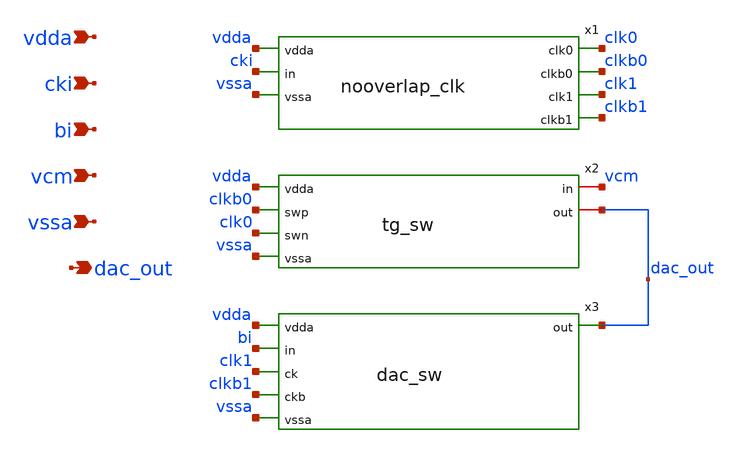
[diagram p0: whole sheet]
** sch_path: xschem/cdac_sw.sch
**.subckt cdac_sw vdda cki bi vcm vssa dac_out
*.ipin vdda
*.ipin cki
*.ipin bi
*.ipin vcm
*.ipin vssa
*.opin dac_out
x1 vdda cki vssa clk0 clkb0 clk1 clkb1 nooverlap_clk
x2 vdda clkb0 clk0 vssa vcm dac_out tg_sw
x3 vdda bi clk1 clkb1 vssa dac_out dac_sw
**.ends

* expanding   symbol:  nooverlap_clk.sym # of pins=7
** sym_path: nooverlap_clk.sym
** sch_path: nooverlap_clk.sch
.subckt nooverlap_clk vdda in vssa clk0 clkb0 clk1 clkb1
*.ipin vdda
*.ipin in
*.ipin vssa
*.opin clk0
*.opin clkb0
*.opin clk1
*.opin clkb1
x1 in a vssa vssa vdda vdda net9 sky130_fd_sc_hd__nand2_1
x2 b net1 vssa vssa vdda vdda net2 sky130_fd_sc_hd__nand2_1
x3 in vssa vssa vdda vdda net1 sky130_fd_sc_hd__inv_1
x4 net9 vssa vssa vdda vdda net8 sky130_fd_sc_hd__inv_1
x5 net2 vssa vssa vdda vdda net3 sky130_fd_sc_hd__inv_1
x6 net8 vssa vssa vdda vdda net7 sky130_fd_sc_hd__inv_1
x7 net3 vssa vssa vdda vdda net4 sky130_fd_sc_hd__inv_1
x8 net7 vssa vssa vdda vdda net6 sky130_fd_sc_hd__inv_4
x9 net4 vssa vssa vdda vdda net5 sky130_fd_sc_hd__inv_4
x10 net10 vssa vssa vdda vdda clkb0 sky130_fd_sc_hd__inv_8
x11 net11 vssa vssa vdda vdda clkb1 sky130_fd_sc_hd__inv_8
x12 clkb0 vssa vssa vdda vdda clk0 sky130_fd_sc_hd__inv_8
x13 clkb1 vssa vssa vdda vdda clk1 sky130_fd_sc_hd__inv_8
x14 net6 vssa vssa vdda vdda b sky130_fd_sc_hd__inv_8
x15 net5 vssa vssa vdda vdda a sky130_fd_sc_hd__inv_8
x16 a vssa vssa vdda vdda net11 sky130_fd_sc_hd__inv_8
x17 b vssa vssa vdda vdda net10 sky130_fd_sc_hd__inv_8
.ends


* expanding   symbol:  tg_sw.sym # of pins=6
** sym_path: tg_sw.sym
** sch_path: tg_sw.sch
.subckt tg_sw vdda swp swn vssa in out
*.ipin vdda
*.ipin swp
*.ipin swn
*.ipin vssa
*.iopin in
*.iopin out
XM1 in swp out vssa sky130_fd_pr__nfet_01v8 L=0.15 W=3 nf=1 ad='int((nf+1)/2) * W/nf * 0.29' as='int((nf+2)/2) * W/nf * 0.29'
+ pd='2*int((nf+1)/2) * (W/nf + 0.29)' ps='2*int((nf+2)/2) * (W/nf + 0.29)' nrd='0.29 / W' nrs='0.29 / W'
+ sa=0 sb=0 sd=0 mult=1 m=1
XM2 in swn out vdda sky130_fd_pr__pfet_01v8 L=0.15 W=9 nf=1 ad='int((nf+1)/2) * W/nf * 0.29' as='int((nf+2)/2) * W/nf * 0.29'
+ pd='2*int((nf+1)/2) * (W/nf + 0.29)' ps='2*int((nf+2)/2) * (W/nf + 0.29)' nrd='0.29 / W' nrs='0.29 / W'
+ sa=0 sb=0 sd=0 mult=1 m=1
.ends


* expanding   symbol:  dac_sw.sym # of pins=6
** sym_path: dac_sw.sym
** sch_path: dac_sw.sch
.subckt dac_sw vdda in ck ckb vssa out
*.ipin vdda
*.ipin in
*.ipin ck
*.ipin ckb
*.ipin vssa
*.opin out
XM1 net1 in vdda vdda sky130_fd_pr__pfet_01v8 L=0.15 W=9 nf=1 ad='int((nf+1)/2) * W/nf * 0.29' as='int((nf+2)/2) * W/nf * 0.29'
+ pd='2*int((nf+1)/2) * (W/nf + 0.29)' ps='2*int((nf+2)/2) * (W/nf + 0.29)' nrd='0.29 / W' nrs='0.29 / W'
+ sa=0 sb=0 sd=0 mult=1 m=1
XM2 out ckb net1 vdda sky130_fd_pr__pfet_01v8 L=0.15 W=9 nf=1 ad='int((nf+1)/2) * W/nf * 0.29' as='int((nf+2)/2) * W/nf * 0.29'
+ pd='2*int((nf+1)/2) * (W/nf + 0.29)' ps='2*int((nf+2)/2) * (W/nf + 0.29)' nrd='0.29 / W' nrs='0.29 / W'
+ sa=0 sb=0 sd=0 mult=1 m=1
XM3 out ck net2 vssa sky130_fd_pr__nfet_01v8 L=0.15 W=3 nf=1 ad='int((nf+1)/2) * W/nf * 0.29' as='int((nf+2)/2) * W/nf * 0.29'
+ pd='2*int((nf+1)/2) * (W/nf + 0.29)' ps='2*int((nf+2)/2) * (W/nf + 0.29)' nrd='0.29 / W' nrs='0.29 / W'
+ sa=0 sb=0 sd=0 mult=1 m=1
XM4 net2 in vssa vssa sky130_fd_pr__nfet_01v8 L=0.15 W=3 nf=1 ad='int((nf+1)/2) * W/nf * 0.29' as='int((nf+2)/2) * W/nf * 0.29'
+ pd='2*int((nf+1)/2) * (W/nf + 0.29)' ps='2*int((nf+2)/2) * (W/nf + 0.29)' nrd='0.29 / W' nrs='0.29 / W'
+ sa=0 sb=0 sd=0 mult=1 m=1
.ends

.end
